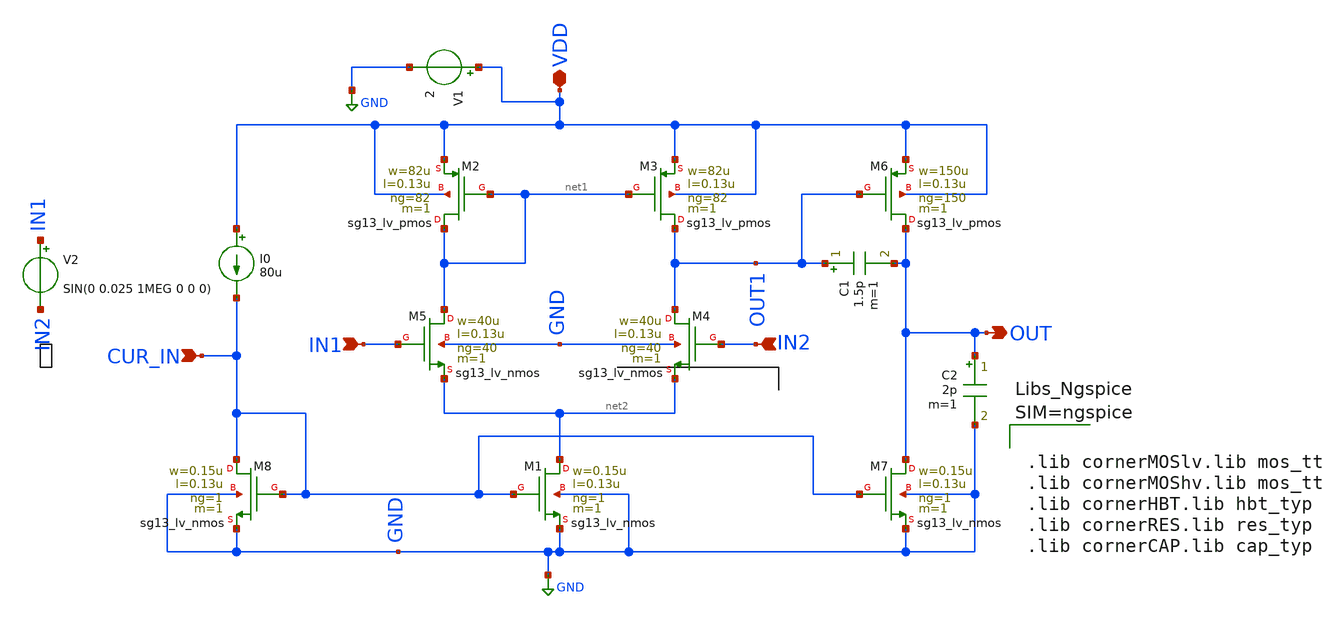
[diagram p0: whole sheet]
** sch_path: opamp_schematic.sch
**.subckt opamp_schematic VDD IN1 IN2 OUT CUR_IN
*.iopin VDD
*.ipin IN1
*.ipin IN2
*.opin OUT
*.ipin CUR_IN
XM1 net2 CUR_IN GND GND sg13_lv_nmos w=0.15u l=0.13u ng=1 m=1 mm_ok=1
XM2 net1 net1 VDD VDD sg13_lv_pmos w=82u l=0.13u ng=82 m=1 mm_ok=1
XM3 OUT1 net1 VDD VDD sg13_lv_pmos w=82u l=0.13u ng=82 m=1 mm_ok=1
XM4 OUT1 IN2 net2 GND sg13_lv_nmos w=40u l=0.13u ng=40 m=1 mm_ok=1
XM5 net1 IN1 net2 GND sg13_lv_nmos w=40u l=0.13u ng=40 m=1 mm_ok=1
XM6 OUT OUT1 VDD VDD sg13_lv_pmos w=150u l=0.13u ng=150 m=1 mm_ok=1
XM7 OUT CUR_IN GND GND sg13_lv_nmos w=0.15u l=0.13u ng=1 m=1 mm_ok=1
XM8 CUR_IN CUR_IN GND GND sg13_lv_nmos w=0.15u l=0.13u ng=1 m=1 mm_ok=1
I0 VDD CUR_IN 80u
V1 VDD GND 2
V2 IN1 IN2 SIN(0 0.025 1MEG 0 0 0)
C1 OUT1 OUT 1.5p m=1
C2 OUT GND 2p m=1
**** begin user architecture code



.lib cornerMOSlv.lib mos_tt
.lib cornerMOShv.lib mos_tt
.lib cornerHBT.lib hbt_typ
.lib cornerRES.lib res_typ
.lib cornerCAP.lib cap_typ



**** end user architecture code
**.ends
.GLOBAL GND
.end
